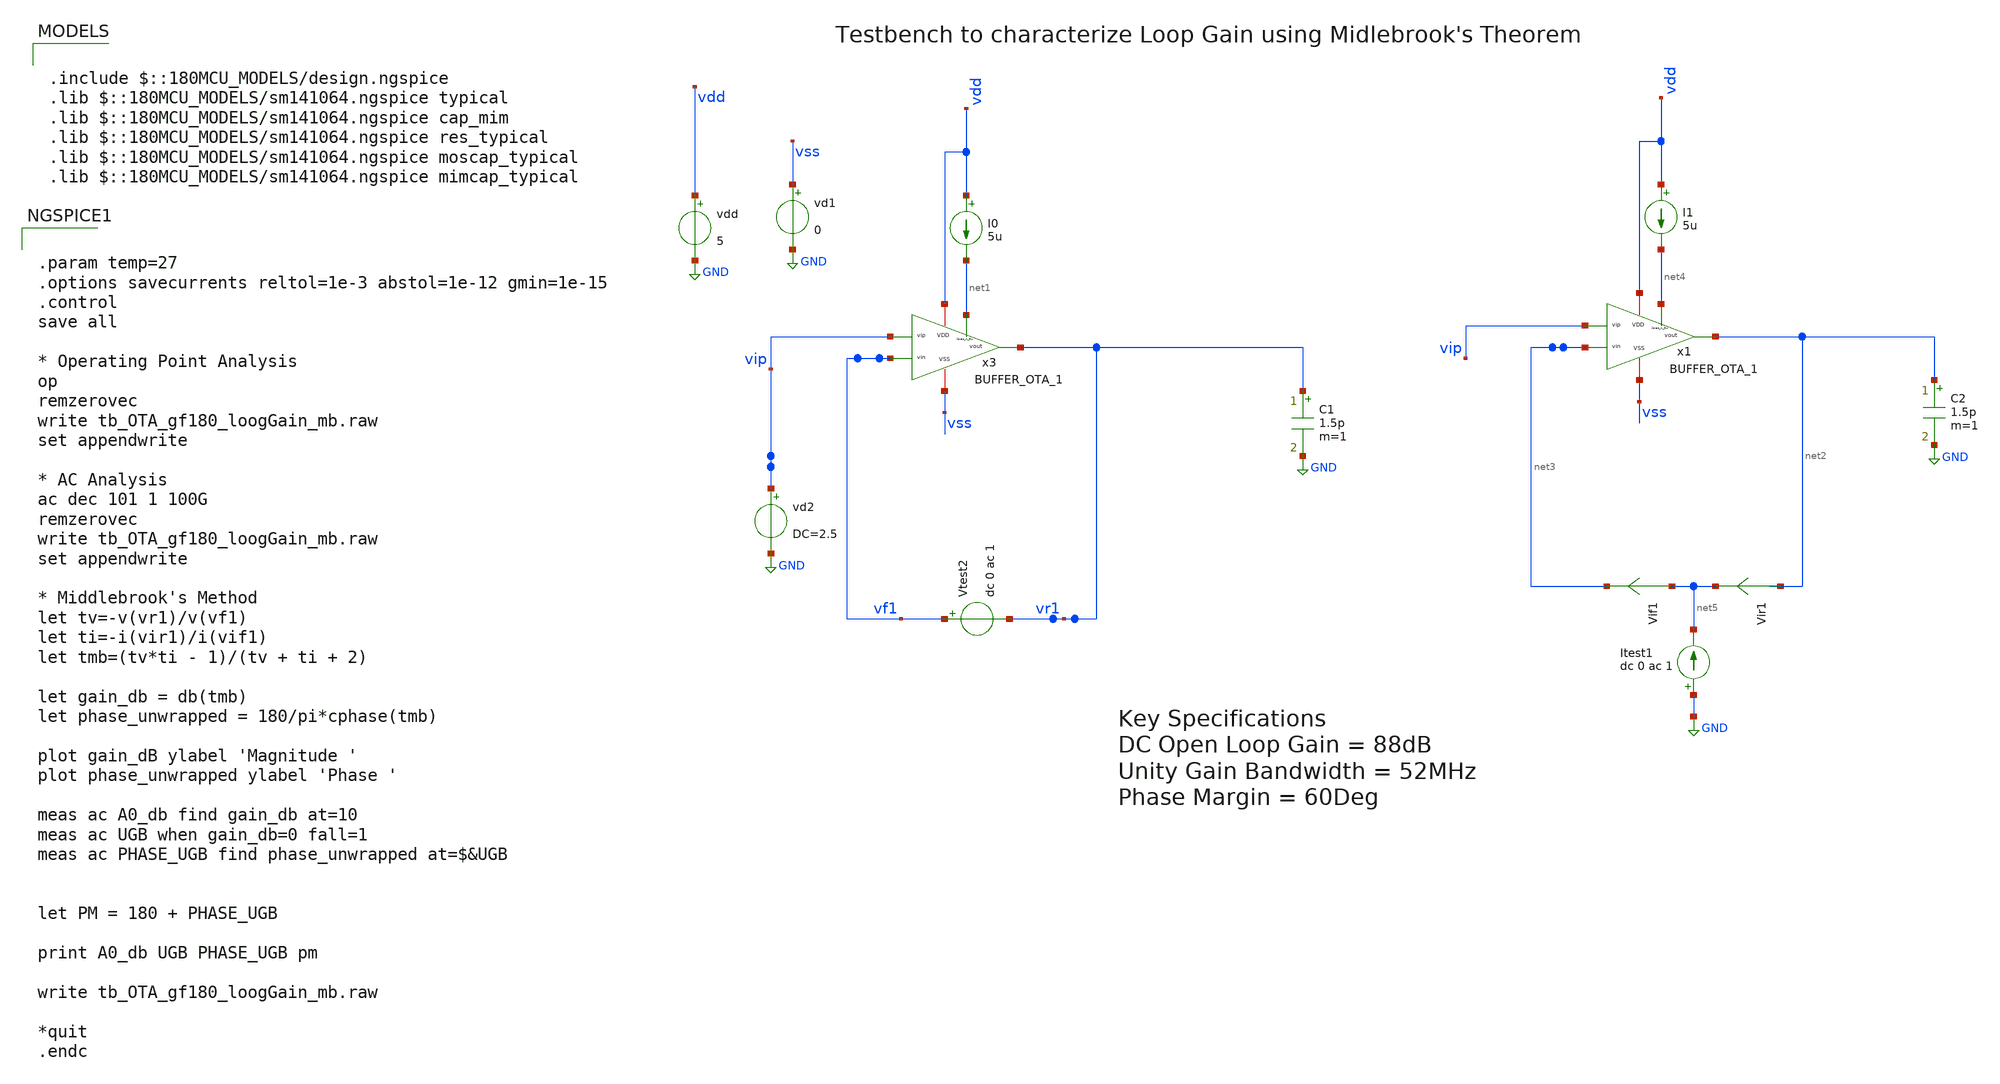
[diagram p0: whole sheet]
** sch_path: xschem/tb_OTA_gf180_loopGain_mb.sch
**.subckt tb_OTA_gf180_loopGain_mb
vdd vdd GND 5
vd1 vss GND 0
vd2 vip GND DC=2.5
C1 vr1 GND 1.5p m=1
I0 vdd net1 5u
C2 net2 GND 1.5p m=1
I1 vdd net4 5u
Vtest2 vf1 vr1 dc 0 ac 1
Vir1 net2 net5 0
.save i(vir1)
Vif1 net5 net3 0
.save i(vif1)
Itest1 GND net5 dc 0 ac 1
x3 vdd vip vf1 vr1 net1 vss BUFFER_OTA_1
x1 vdd vip net3 net2 net4 vss BUFFER_OTA_1
**** begin user architecture code

.include $::180MCU_MODELS/design.ngspice
.lib $::180MCU_MODELS/sm141064.ngspice typical
.lib $::180MCU_MODELS/sm141064.ngspice cap_mim
.lib $::180MCU_MODELS/sm141064.ngspice res_typical
.lib $::180MCU_MODELS/sm141064.ngspice moscap_typical
.lib $::180MCU_MODELS/sm141064.ngspice mimcap_typical



.param temp=27
.options savecurrents reltol=1e-3 abstol=1e-12 gmin=1e-15
.control
save all

* Operating Point Analysis
op
remzerovec
write tb_OTA_gf180_loogGain_mb.raw
set appendwrite

* AC Analysis
ac dec 101 1 100G
remzerovec
write tb_OTA_gf180_loogGain_mb.raw
set appendwrite

* Middlebrook's Method
let tv=-v(vr1)/v(vf1)
let ti=-i(vir1)/i(vif1)
let tmb=(tv*ti - 1)/(tv + ti + 2)

let gain_db = db(tmb)
let phase_unwrapped = 180/pi*cphase(tmb)

plot gain_dB ylabel 'Magnitude '
plot phase_unwrapped ylabel 'Phase '

meas ac A0_db find gain_db at=10
meas ac UGB when gain_db=0 fall=1
meas ac PHASE_UGB find phase_unwrapped at=$&UGB


let PM = 180 + PHASE_UGB

print A0_db UGB PHASE_UGB pm

write tb_OTA_gf180_loogGain_mb.raw

*quit
.endc


**** end user architecture code
**.ends
.GLOBAL GND
.end
